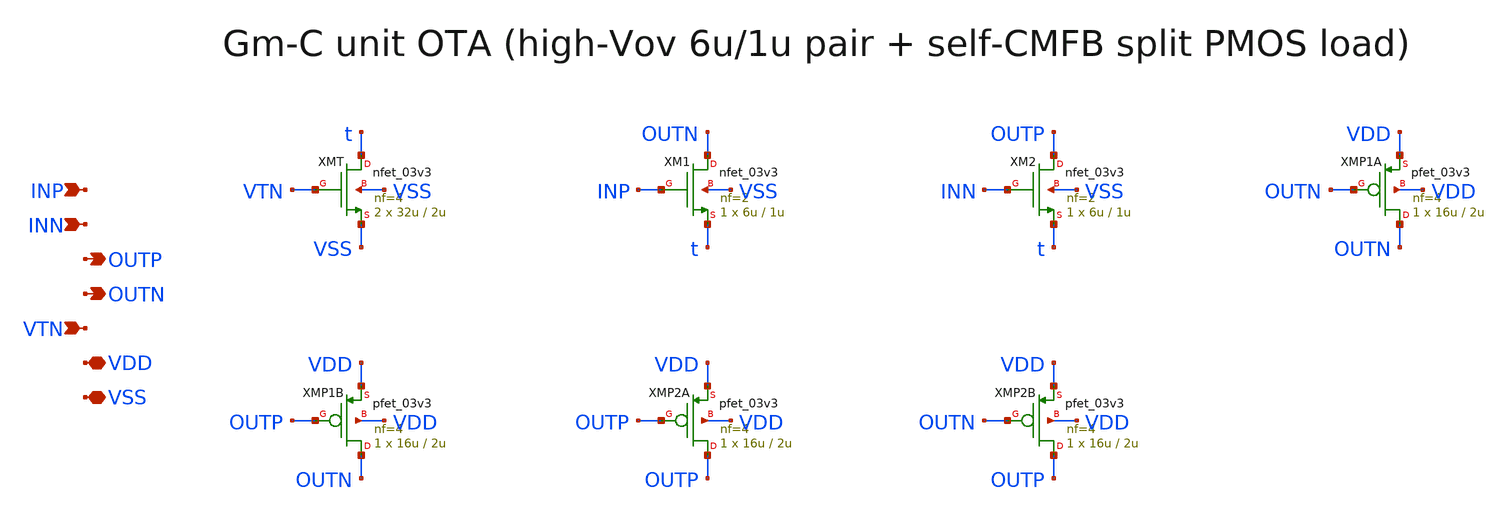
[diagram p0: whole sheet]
** sch_path: xschem/gm_unit.sch
**.subckt gm_unit INP INN OUTP OUTN VTN VDD VSS
*.ipin INP
*.ipin INN
*.opin OUTP
*.opin OUTN
*.ipin VTN
*.iopin VDD
*.iopin VSS
XMT t VTN VSS VSS nfet_03v3 L=2u W=32u nf=4 ad='int((nf+1)/2) * W/nf * 0.18u' as='int((nf+2)/2) * W/nf * 0.18u'
+ pd='2*int((nf+1)/2) * (W/nf + 0.18u)' ps='2*int((nf+2)/2) * (W/nf + 0.18u)' nrd='0.18u / W' nrs='0.18u / W'
+ sa=0 sb=0 sd=0 m=2
XM1 OUTN INP t VSS nfet_03v3 L=1u W=6u nf=2 ad='int((nf+1)/2) * W/nf * 0.18u' as='int((nf+2)/2) * W/nf * 0.18u'
+ pd='2*int((nf+1)/2) * (W/nf + 0.18u)' ps='2*int((nf+2)/2) * (W/nf + 0.18u)' nrd='0.18u / W' nrs='0.18u / W'
+ sa=0 sb=0 sd=0 m=1
XM2 OUTP INN t VSS nfet_03v3 L=1u W=6u nf=2 ad='int((nf+1)/2) * W/nf * 0.18u' as='int((nf+2)/2) * W/nf * 0.18u'
+ pd='2*int((nf+1)/2) * (W/nf + 0.18u)' ps='2*int((nf+2)/2) * (W/nf + 0.18u)' nrd='0.18u / W' nrs='0.18u / W'
+ sa=0 sb=0 sd=0 m=1
XMP1A OUTN OUTN VDD VDD pfet_03v3 L=2u W=16u nf=4 ad='int((nf+1)/2) * W/nf * 0.18u' as='int((nf+2)/2) * W/nf * 0.18u'
+ pd='2*int((nf+1)/2) * (W/nf + 0.18u)' ps='2*int((nf+2)/2) * (W/nf + 0.18u)' nrd='0.18u / W' nrs='0.18u / W'
+ sa=0 sb=0 sd=0 m=1
XMP1B OUTN OUTP VDD VDD pfet_03v3 L=2u W=16u nf=4 ad='int((nf+1)/2) * W/nf * 0.18u' as='int((nf+2)/2) * W/nf * 0.18u'
+ pd='2*int((nf+1)/2) * (W/nf + 0.18u)' ps='2*int((nf+2)/2) * (W/nf + 0.18u)' nrd='0.18u / W' nrs='0.18u / W'
+ sa=0 sb=0 sd=0 m=1
XMP2A OUTP OUTP VDD VDD pfet_03v3 L=2u W=16u nf=4 ad='int((nf+1)/2) * W/nf * 0.18u' as='int((nf+2)/2) * W/nf * 0.18u'
+ pd='2*int((nf+1)/2) * (W/nf + 0.18u)' ps='2*int((nf+2)/2) * (W/nf + 0.18u)' nrd='0.18u / W' nrs='0.18u / W'
+ sa=0 sb=0 sd=0 m=1
XMP2B OUTP OUTN VDD VDD pfet_03v3 L=2u W=16u nf=4 ad='int((nf+1)/2) * W/nf * 0.18u' as='int((nf+2)/2) * W/nf * 0.18u'
+ pd='2*int((nf+1)/2) * (W/nf + 0.18u)' ps='2*int((nf+2)/2) * (W/nf + 0.18u)' nrd='0.18u / W' nrs='0.18u / W'
+ sa=0 sb=0 sd=0 m=1
**.ends
.end
